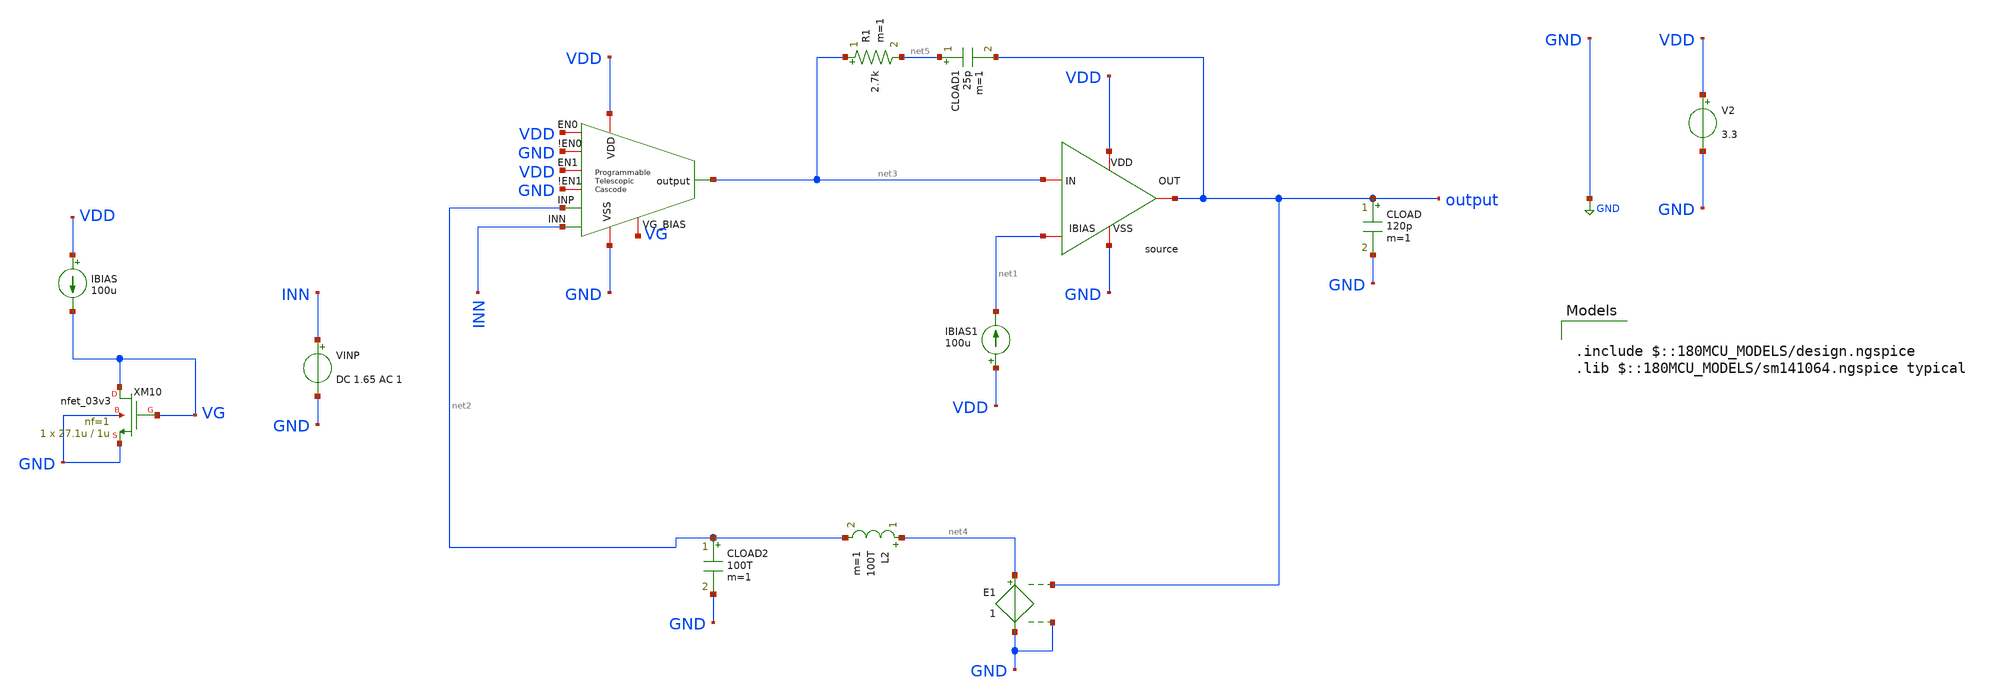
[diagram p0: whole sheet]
** sch_path: designs/libs/core_amps/two_stage_amps/tele_cs_ac_comp_tb.sch
**.subckt tele_cs_ac_comp_tb
V2 VDD GND 3.3
IBIAS1 VDD net1 100u
CLOAD output GND 120p m=1
VINP INN GND DC 1.65 AC 1
L2 net4 net2 100T m=1
CLOAD2 net2 GND 100T m=1
E1 net4 GND output GND 1
CLOAD1 net5 output 25p m=1
R1 net3 net5 2.7k m=1
x2 VDD net3 net1 output GND cs_schematic
x1 VDD net3 VDD GND VDD GND INN net2 GND VG programmable_telescopic_cascode
IBIAS VDD VG 100u
XM10 VG VG GND GND nfet_03v3 L=1u W=27.1u nf=1 ad='int((nf+1)/2) * W/nf * 0.18u' as='int((nf+2)/2) * W/nf * 0.18u'
+ pd='2*int((nf+1)/2) * (W/nf + 0.18u)' ps='2*int((nf+2)/2) * (W/nf + 0.18u)' nrd='0.18u / W' nrs='0.18u / W'
+ sa=0 sb=0 sd=0 m=1
**** begin user architecture code

.include $::180MCU_MODELS/design.ngspice
.lib $::180MCU_MODELS/sm141064.ngspice typical



.control
ac dec 100 1 10G

let gain_db = vdb(output)
let phase = 180 * vp(output) / 3.14159

meas ac a0_db find gain_db at=1

let thresh3 = a0_db - 3
let thresh6 = a0_db - 6

meas ac fp1 when gain_db=thresh3 fall=1
meas ac fp2_est when gain_db=thresh6 fall=1

meas ac ugf when gain_db=0 fall=1
meas ac phase_ugf find phase at=ugf

let phase_margin = 180 + phase_ugf
if (phase_margin > 180)
  let phase_margin = phase_margin - 360
end

print phase_margin

plot gain_db
plot phase
.endc



**** end user architecture code
**.ends
.GLOBAL GND
.end
